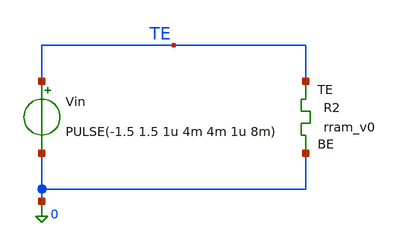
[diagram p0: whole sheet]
** sch_path: memristor_models/wellposed/tb_rram_v0.sch
**.subckt tb_rram_v0
Vin TE 0 PULSE(-1.5 1.5 1u 4m 4m 1u 8m)
XR2 TE 0 rram_v0
**** begin user architecture code

** opencircuitdesign pdks install
.inc $::SKYWATER_MODELS/rram_v0.spice



.tran 1e-6 8m
.options savecurrents
.control
run
save all
write tb_rram_v0.raw
.endc


**** end user architecture code
**.ends
.end
